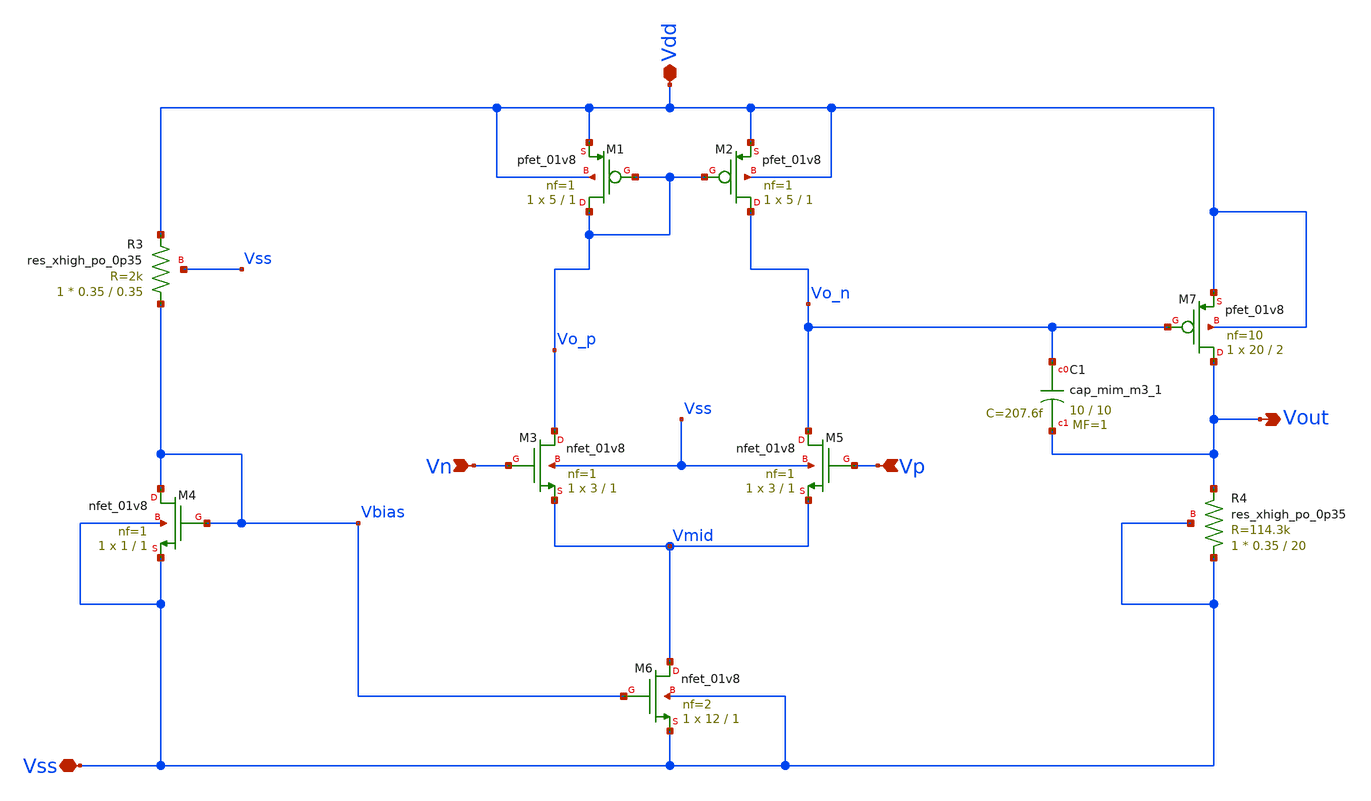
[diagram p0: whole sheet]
** sch_path: Circuits/DiffAmp/TwoStageDiffAmp_flat.sch
**.subckt TwoStageDiffAmp_flat Vss Vn Vp Vout Vdd
*.iopin Vss
*.ipin Vn
*.ipin Vp
*.opin Vout
*.iopin Vdd
XR3 Vbias Vdd Vss sky130_fd_pr__res_xhigh_po_0p35 L=0.35 mult=1 m=1
XM4 Vbias Vbias Vss Vss sky130_fd_pr__nfet_01v8 L=1 W=1 nf=1 ad='int((nf+1)/2) * W/nf * 0.29' as='int((nf+2)/2) * W/nf * 0.29'
+ pd='2*int((nf+1)/2) * (W/nf + 0.29)' ps='2*int((nf+2)/2) * (W/nf + 0.29)' nrd='0.29 / W' nrs='0.29 / W'
+ sa=0 sb=0 sd=0 mult=1 m=1
XM1 Vo_p Vo_p Vdd Vdd sky130_fd_pr__pfet_01v8 L=1 W=5 nf=1 ad='int((nf+1)/2) * W/nf * 0.29' as='int((nf+2)/2) * W/nf * 0.29'
+ pd='2*int((nf+1)/2) * (W/nf + 0.29)' ps='2*int((nf+2)/2) * (W/nf + 0.29)' nrd='0.29 / W' nrs='0.29 / W'
+ sa=0 sb=0 sd=0 mult=1 m=1
XM2 Vo_n Vo_p Vdd Vdd sky130_fd_pr__pfet_01v8 L=1 W=5 nf=1 ad='int((nf+1)/2) * W/nf * 0.29' as='int((nf+2)/2) * W/nf * 0.29'
+ pd='2*int((nf+1)/2) * (W/nf + 0.29)' ps='2*int((nf+2)/2) * (W/nf + 0.29)' nrd='0.29 / W' nrs='0.29 / W'
+ sa=0 sb=0 sd=0 mult=1 m=1
XM3 Vo_p Vn Vmid Vss sky130_fd_pr__nfet_01v8 L=1 W=3 nf=1 ad='int((nf+1)/2) * W/nf * 0.29' as='int((nf+2)/2) * W/nf * 0.29'
+ pd='2*int((nf+1)/2) * (W/nf + 0.29)' ps='2*int((nf+2)/2) * (W/nf + 0.29)' nrd='0.29 / W' nrs='0.29 / W'
+ sa=0 sb=0 sd=0 mult=1 m=1
XM5 Vo_n Vp Vmid Vss sky130_fd_pr__nfet_01v8 L=1 W=3 nf=1 ad='int((nf+1)/2) * W/nf * 0.29' as='int((nf+2)/2) * W/nf * 0.29'
+ pd='2*int((nf+1)/2) * (W/nf + 0.29)' ps='2*int((nf+2)/2) * (W/nf + 0.29)' nrd='0.29 / W' nrs='0.29 / W'
+ sa=0 sb=0 sd=0 mult=1 m=1
XM6 Vmid Vbias Vss Vss sky130_fd_pr__nfet_01v8 L=1 W=12 nf=2 ad='int((nf+1)/2) * W/nf * 0.29' as='int((nf+2)/2) * W/nf * 0.29'
+ pd='2*int((nf+1)/2) * (W/nf + 0.29)' ps='2*int((nf+2)/2) * (W/nf + 0.29)' nrd='0.29 / W' nrs='0.29 / W'
+ sa=0 sb=0 sd=0 mult=1 m=1
XM7 Vout Vo_n Vdd Vdd sky130_fd_pr__pfet_01v8 L=2 W=20 nf=10 ad='int((nf+1)/2) * W/nf * 0.29' as='int((nf+2)/2) * W/nf * 0.29'
+ pd='2*int((nf+1)/2) * (W/nf + 0.29)' ps='2*int((nf+2)/2) * (W/nf + 0.29)' nrd='0.29 / W' nrs='0.29 / W'
+ sa=0 sb=0 sd=0 mult=1 m=1
XR4 Vss Vout Vss sky130_fd_pr__res_xhigh_po_0p35 L=20 mult=1 m=1
XC1 Vo_n Vout sky130_fd_pr__cap_mim_m3_1 W=10 L=10 MF=1 m=1
**.ends
.end
